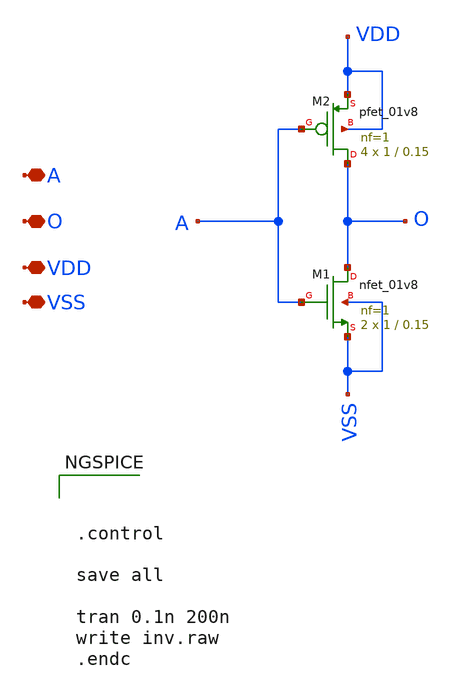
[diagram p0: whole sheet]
** sch_path: inv.sch
**.subckt inv A O VDD VSS
*.iopin A
*.iopin O
*.iopin VDD
*.iopin VSS
XM1 O A VSS VSS sky130_fd_pr__nfet_01v8 L=0.15 W=1 nf=1 ad='int((nf+1)/2) * W/nf * 0.29' as='int((nf+2)/2) * W/nf * 0.29'
+ pd='2*int((nf+1)/2) * (W/nf + 0.29)' ps='2*int((nf+2)/2) * (W/nf + 0.29)' nrd='0.29 / W' nrs='0.29 / W'
+ sa=0 sb=0 sd=0 mult=2 m=2
XM2 O A VDD VDD sky130_fd_pr__pfet_01v8 L=0.15 W=1 nf=1 ad='int((nf+1)/2) * W/nf * 0.29' as='int((nf+2)/2) * W/nf * 0.29'
+ pd='2*int((nf+1)/2) * (W/nf + 0.29)' ps='2*int((nf+2)/2) * (W/nf + 0.29)' nrd='0.29 / W' nrs='0.29 / W'
+ sa=0 sb=0 sd=0 mult=4 m=4
**** begin user architecture code

** opencircuitdesign pdks install
.lib $::SKYWATER_MODELS/sky130.lib.spice tt_mm





.control

save all

tran 0.1n 200n
write inv.raw
.endc


**** end user architecture code
**.ends
.end
